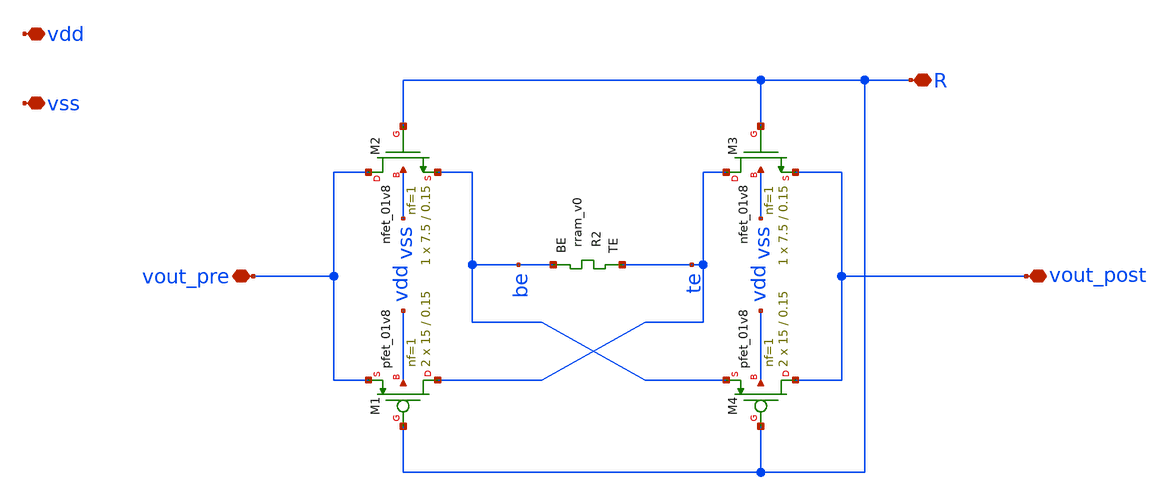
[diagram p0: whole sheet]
** sch_path: Synapse/rstdp_switched.sch
**.subckt rstdp_switched vdd vss R vout_post vout_pre
*.iopin vdd
*.iopin vss
*.iopin R
*.iopin vout_post
*.iopin vout_pre
XR2 te be rram_v0
XM2 vout_pre R be vss sky130_fd_pr__nfet_01v8 L=0.15 W=7.5 nf=1 ad='int((nf+1)/2) * W/nf * 0.29' as='int((nf+2)/2) * W/nf * 0.29'
+ pd='2*int((nf+1)/2) * (W/nf + 0.29)' ps='2*int((nf+2)/2) * (W/nf + 0.29)' nrd='0.29 / W' nrs='0.29 / W'
+ sa=0 sb=0 sd=0 mult=1 m=1
XM3 te R vout_post vss sky130_fd_pr__nfet_01v8 L=0.15 W=7.5 nf=1 ad='int((nf+1)/2) * W/nf * 0.29' as='int((nf+2)/2) * W/nf * 0.29'
+ pd='2*int((nf+1)/2) * (W/nf + 0.29)' ps='2*int((nf+2)/2) * (W/nf + 0.29)' nrd='0.29 / W' nrs='0.29 / W'
+ sa=0 sb=0 sd=0 mult=1 m=1
XM1 te R vout_pre vdd sky130_fd_pr__pfet_01v8 L=0.15 W=15 nf=1 ad='int((nf+1)/2) * W/nf * 0.29' as='int((nf+2)/2) * W/nf * 0.29'
+ pd='2*int((nf+1)/2) * (W/nf + 0.29)' ps='2*int((nf+2)/2) * (W/nf + 0.29)' nrd='0.29 / W' nrs='0.29 / W'
+ sa=0 sb=0 sd=0 mult=2 m=2
XM4 vout_post R be vdd sky130_fd_pr__pfet_01v8 L=0.15 W=15 nf=1 ad='int((nf+1)/2) * W/nf * 0.29' as='int((nf+2)/2) * W/nf * 0.29'
+ pd='2*int((nf+1)/2) * (W/nf + 0.29)' ps='2*int((nf+2)/2) * (W/nf + 0.29)' nrd='0.29 / W' nrs='0.29 / W'
+ sa=0 sb=0 sd=0 mult=2 m=2
**.ends
.end
